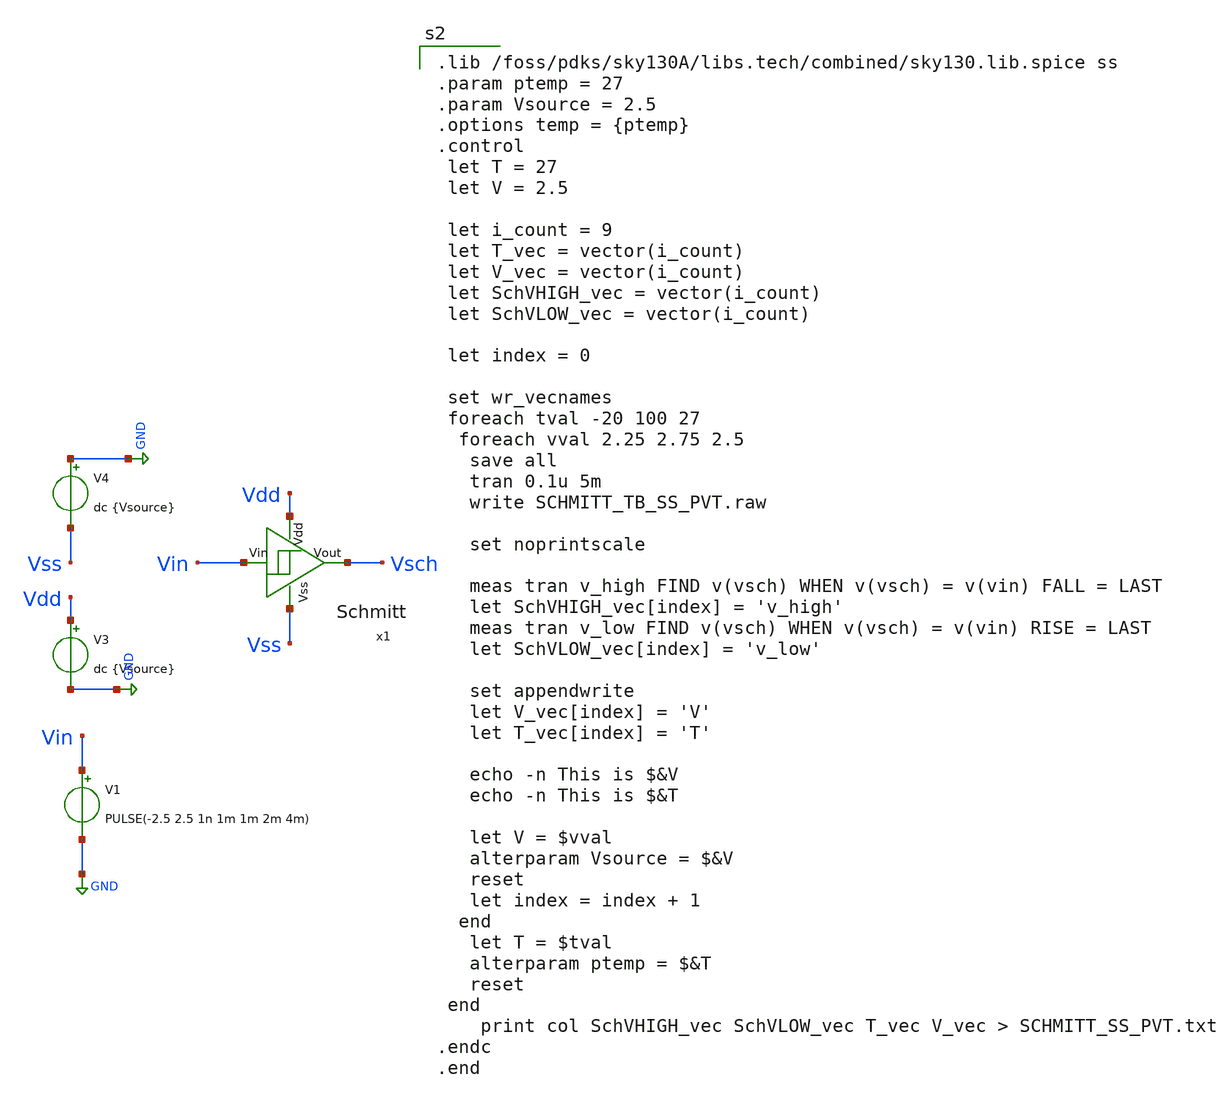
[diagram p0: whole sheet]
** sch_path: xschem/Schmitt_TB.sch
**.subckt Schmitt_TB
x1 Vdd Vss Vin Vsch Schmitt
V4 GND Vss dc {Vsource}
V3 Vdd GND dc {Vsource}
V1 Vin GND PULSE(-2.5 2.5 1n 1m 1m 2m 4m)
**** begin user architecture code

.lib /foss/pdks/sky130A/libs.tech/combined/sky130.lib.spice ss
.param ptemp = 27
.param Vsource = 2.5
.options temp = {ptemp}
.control
 let T = 27
 let V = 2.5

 let i_count = 9
 let T_vec = vector(i_count)
 let V_vec = vector(i_count)
 let SchVHIGH_vec = vector(i_count)
 let SchVLOW_vec = vector(i_count)

 let index = 0

 set wr_vecnames
 foreach tval -20 100 27
  foreach vval 2.25 2.75 2.5
   save all
   tran 0.1u 5m
   write SCHMITT_TB_SS_PVT.raw

   set noprintscale

   meas tran v_high FIND v(vsch) WHEN v(vsch) = v(vin) FALL = LAST
   let SchVHIGH_vec[index] = 'v_high'
   meas tran v_low FIND v(vsch) WHEN v(vsch) = v(vin) RISE = LAST
   let SchVLOW_vec[index] = 'v_low'

   set appendwrite
   let V_vec[index] = 'V'
   let T_vec[index] = 'T'

   echo -n This is $&V
   echo -n This is $&T

   let V = $vval
   alterparam Vsource = $&V
   reset
   let index = index + 1
  end
   let T = $tval
   alterparam ptemp = $&T
   reset
 end
    print col SchVHIGH_vec SchVLOW_vec T_vec V_vec > SCHMITT_SS_PVT.txt
.endc
.end


**** end user architecture code
**.ends

* expanding   symbol:  Schmitt.sym # of pins=4
** sym_path: xschem/Schmitt.sym
** sch_path: xschem/Schmitt.sch
.subckt Schmitt Vdd Vss Vin Vout
*.opin Vout
*.ipin Vin
*.ipin Vdd
*.ipin Vss
XM1 net1 Vin Vss Vss sky130_fd_pr__nfet_g5v0d10v5 L=0.5 W=2.92 nf=1 ad='int((1 + 1)/2) * 2.92 / 1 * 0.29'
+ as='int((1 + 2)/2) * 2.92 / 1 * 0.29' pd='2*int((1 + 1)/2) * (2.92 / 1 + 0.29)' ps='2*int((1 + 2)/2) * (2.92 / 1 + 0.29)'
+ nrd='0.29 / 2.92 ' nrs='0.29 / 2.92 ' sa=0 sb=0 sd=0 mult=1 m=1
XM5 net2 Vin Vdd Vdd sky130_fd_pr__pfet_g5v0d10v5 L=0.5 W=9.78 nf=1 ad='int((1 + 1)/2) * 9.78 / 1 * 0.29'
+ as='int((1 + 2)/2) * 9.78 / 1 * 0.29' pd='2*int((1 + 1)/2) * (9.78 / 1 + 0.29)' ps='2*int((1 + 2)/2) * (9.78 / 1 + 0.29)'
+ nrd='0.29 / 9.78 ' nrs='0.29 / 9.78 ' sa=0 sb=0 sd=0 mult=1 m=1
XM3 Vdd Vout net1 Vss sky130_fd_pr__nfet_g5v0d10v5 L=0.5 W=1 nf=1 ad='int((1 + 1)/2) * 1 / 1 * 0.29'
+ as='int((1 + 2)/2) * 1 / 1 * 0.29' pd='2*int((1 + 1)/2) * (1 / 1 + 0.29)' ps='2*int((1 + 2)/2) * (1 / 1 + 0.29)'
+ nrd='0.29 / 1 ' nrs='0.29 / 1 ' sa=0 sb=0 sd=0 mult=1 m=1
XM2 Vout Vin net1 Vss sky130_fd_pr__nfet_g5v0d10v5 L=0.5 W=4 nf=1 ad='int((1 + 1)/2) * 4 / 1 * 0.29'
+ as='int((1 + 2)/2) * 4 / 1 * 0.29' pd='2*int((1 + 1)/2) * (4 / 1 + 0.29)' ps='2*int((1 + 2)/2) * (4 / 1 + 0.29)'
+ nrd='0.29 / 4 ' nrs='0.29 / 4 ' sa=0 sb=0 sd=0 mult=1 m=1
XM6 Vss Vout net2 Vdd sky130_fd_pr__pfet_g5v0d10v5 L=0.5 W=3 nf=1 ad='int((1 + 1)/2) * 3 / 1 * 0.29'
+ as='int((1 + 2)/2) * 3 / 1 * 0.29' pd='2*int((1 + 1)/2) * (3 / 1 + 0.29)' ps='2*int((1 + 2)/2) * (3 / 1 + 0.29)'
+ nrd='0.29 / 3 ' nrs='0.29 / 3 ' sa=0 sb=0 sd=0 mult=1 m=1
XM4 Vout Vin net2 Vdd sky130_fd_pr__pfet_g5v0d10v5 L=0.5 W=12 nf=1 ad='int((1 + 1)/2) * 12 / 1 * 0.29'
+ as='int((1 + 2)/2) * 12 / 1 * 0.29' pd='2*int((1 + 1)/2) * (12 / 1 + 0.29)' ps='2*int((1 + 2)/2) * (12 / 1 + 0.29)'
+ nrd='0.29 / 12 ' nrs='0.29 / 12 ' sa=0 sb=0 sd=0 mult=1 m=1
.ends

.GLOBAL GND
.end
